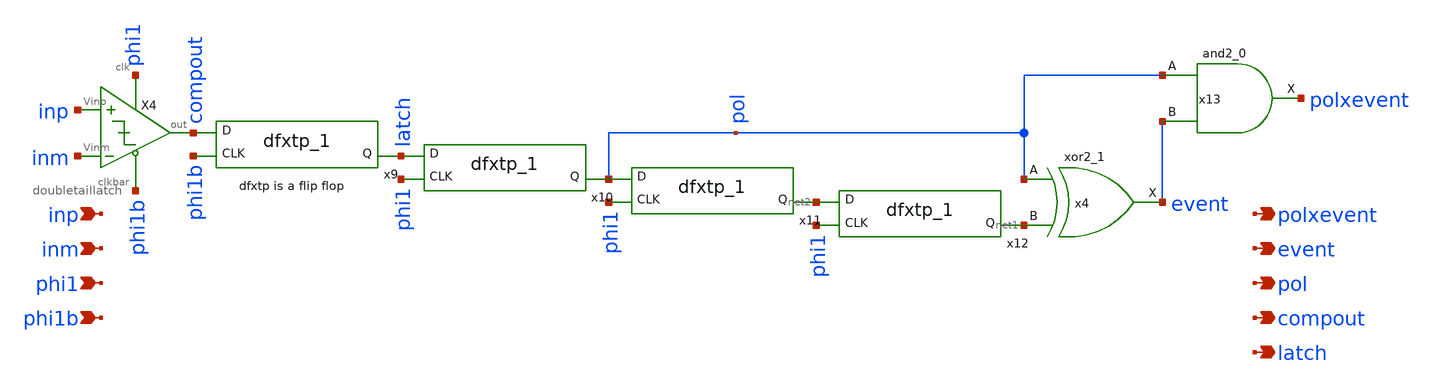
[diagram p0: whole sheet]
** sch_path: xschem/comparator/comparator_out.sch
**.subckt comparator_out inp event polxevent pol inm phi1 phi1b compout latch
*.ipin inp
*.opin event
*.opin polxevent
*.opin pol
*.ipin inm
*.ipin phi1
*.ipin phi1b
*.opin compout
*.opin latch
X4 inp inm compout phi1 phi1b doubletaillatch
x4 pol net1 GND GND VDD VDD event sky130_fd_sc_lp__xor2_1
x11 phi1 pol gnd gnd vdd vdd net2 sky130_fd_sc_lp__dfxtp_1
x12 phi1 net2 gnd gnd vdd vdd net1 sky130_fd_sc_lp__dfxtp_1
x9 phi1b compout gnd gnd vdd vdd latch sky130_fd_sc_lp__dfxtp_1
x10 phi1 latch gnd gnd vdd vdd pol sky130_fd_sc_lp__dfxtp_1
x13 pol event GND GND VDD VDD polxevent sky130_fd_sc_lp__and2_0
**.ends

* expanding   symbol:  comparator/doubletaillatch.sym # of pins=5
** sym_path: xschem/comparator/doubletaillatch.sym
** sch_path: xschem/comparator/doubletaillatch.sch
.subckt doubletaillatch Vinp Vinm out clk clkbar
*.ipin clkbar
*.opin out
*.ipin Vinp
*.ipin Vinm
*.ipin clk
XM3 net6 out VDD VDD sky130_fd_pr__pfet_01v8 L=1 W=4 nf=1 ad='int((nf+1)/2) * W/nf * 0.29' as='int((nf+2)/2) * W/nf * 0.29'
+ pd='2*int((nf+1)/2) * (W/nf + 0.29)' ps='2*int((nf+2)/2) * (W/nf + 0.29)' nrd='0.29 / W' nrs='0.29 / W'
+ sa=0 sb=0 sd=0 mult=1 m=1
XM4 VDD net1 net7 VDD sky130_fd_pr__pfet_01v8 L=1 W=4 nf=1 ad='int((nf+1)/2) * W/nf * 0.29' as='int((nf+2)/2) * W/nf * 0.29'
+ pd='2*int((nf+1)/2) * (W/nf + 0.29)' ps='2*int((nf+2)/2) * (W/nf + 0.29)' nrd='0.29 / W' nrs='0.29 / W'
+ sa=0 sb=0 sd=0 mult=1 m=1
XM5 net7 net3 out VDD sky130_fd_pr__pfet_01v8 L=1 W=4 nf=1 ad='int((nf+1)/2) * W/nf * 0.29' as='int((nf+2)/2) * W/nf * 0.29'
+ pd='2*int((nf+1)/2) * (W/nf + 0.29)' ps='2*int((nf+2)/2) * (W/nf + 0.29)' nrd='0.29 / W' nrs='0.29 / W'
+ sa=0 sb=0 sd=0 mult=1 m=1
XM6 net1 net4 net6 VDD sky130_fd_pr__pfet_01v8 L=1 W=4 nf=1 ad='int((nf+1)/2) * W/nf * 0.29' as='int((nf+2)/2) * W/nf * 0.29'
+ pd='2*int((nf+1)/2) * (W/nf + 0.29)' ps='2*int((nf+2)/2) * (W/nf + 0.29)' nrd='0.29 / W' nrs='0.29 / W'
+ sa=0 sb=0 sd=0 mult=1 m=1
XM7 out clkbar GND GND sky130_fd_pr__nfet_01v8 L=1 W=2 nf=1 ad='int((nf+1)/2) * W/nf * 0.29' as='int((nf+2)/2) * W/nf * 0.29'
+ pd='2*int((nf+1)/2) * (W/nf + 0.29)' ps='2*int((nf+2)/2) * (W/nf + 0.29)' nrd='0.29 / W' nrs='0.29 / W'
+ sa=0 sb=0 sd=0 mult=1 m=1
XM8 GND net1 out GND sky130_fd_pr__nfet_01v8 L=1 W=2 nf=1 ad='int((nf+1)/2) * W/nf * 0.29' as='int((nf+2)/2) * W/nf * 0.29'
+ pd='2*int((nf+1)/2) * (W/nf + 0.29)' ps='2*int((nf+2)/2) * (W/nf + 0.29)' nrd='0.29 / W' nrs='0.29 / W'
+ sa=0 sb=0 sd=0 mult=1 m=1
XM9 net1 out GND GND sky130_fd_pr__nfet_01v8 L=1 W=2 nf=1 ad='int((nf+1)/2) * W/nf * 0.29' as='int((nf+2)/2) * W/nf * 0.29'
+ pd='2*int((nf+1)/2) * (W/nf + 0.29)' ps='2*int((nf+2)/2) * (W/nf + 0.29)' nrd='0.29 / W' nrs='0.29 / W'
+ sa=0 sb=0 sd=0 mult=1 m=1
XM10 GND clkbar net1 GND sky130_fd_pr__nfet_01v8 L=1 W=2 nf=1 ad='int((nf+1)/2) * W/nf * 0.29' as='int((nf+2)/2) * W/nf * 0.29'
+ pd='2*int((nf+1)/2) * (W/nf + 0.29)' ps='2*int((nf+2)/2) * (W/nf + 0.29)' nrd='0.29 / W' nrs='0.29 / W'
+ sa=0 sb=0 sd=0 mult=1 m=1
XM11 net4 clk VDD VDD sky130_fd_pr__pfet_01v8 L=1 W=4 nf=1 ad='int((nf+1)/2) * W/nf * 0.29' as='int((nf+2)/2) * W/nf * 0.29'
+ pd='2*int((nf+1)/2) * (W/nf + 0.29)' ps='2*int((nf+2)/2) * (W/nf + 0.29)' nrd='0.29 / W' nrs='0.29 / W'
+ sa=0 sb=0 sd=0 mult=1 m=1
XM12 VDD clk net3 VDD sky130_fd_pr__pfet_01v8 L=1 W=4 nf=1 ad='int((nf+1)/2) * W/nf * 0.29' as='int((nf+2)/2) * W/nf * 0.29'
+ pd='2*int((nf+1)/2) * (W/nf + 0.29)' ps='2*int((nf+2)/2) * (W/nf + 0.29)' nrd='0.29 / W' nrs='0.29 / W'
+ sa=0 sb=0 sd=0 mult=1 m=1
XM13 net4 Vinm net2 GND sky130_fd_pr__nfet_01v8 L=1 W=2 nf=1 ad='int((nf+1)/2) * W/nf * 0.29' as='int((nf+2)/2) * W/nf * 0.29'
+ pd='2*int((nf+1)/2) * (W/nf + 0.29)' ps='2*int((nf+2)/2) * (W/nf + 0.29)' nrd='0.29 / W' nrs='0.29 / W'
+ sa=0 sb=0 sd=0 mult=1 m=1
XM14 net2 Vinp net3 GND sky130_fd_pr__nfet_01v8 L=1 W=2 nf=1 ad='int((nf+1)/2) * W/nf * 0.29' as='int((nf+2)/2) * W/nf * 0.29'
+ pd='2*int((nf+1)/2) * (W/nf + 0.29)' ps='2*int((nf+2)/2) * (W/nf + 0.29)' nrd='0.29 / W' nrs='0.29 / W'
+ sa=0 sb=0 sd=0 mult=1 m=1
XM15 net2 clk net5 GND sky130_fd_pr__nfet_01v8 L=1 W=2 nf=1 ad='int((nf+1)/2) * W/nf * 0.29' as='int((nf+2)/2) * W/nf * 0.29'
+ pd='2*int((nf+1)/2) * (W/nf + 0.29)' ps='2*int((nf+2)/2) * (W/nf + 0.29)' nrd='0.29 / W' nrs='0.29 / W'
+ sa=0 sb=0 sd=0 mult=1 m=1
XM16 net5 clkbar GND GND sky130_fd_pr__nfet_01v8 L=1 W=2 nf=1 ad='int((nf+1)/2) * W/nf * 0.29' as='int((nf+2)/2) * W/nf * 0.29'
+ pd='2*int((nf+1)/2) * (W/nf + 0.29)' ps='2*int((nf+2)/2) * (W/nf + 0.29)' nrd='0.29 / W' nrs='0.29 / W'
+ sa=0 sb=0 sd=0 mult=1 m=1
XC2 net5 GND sky130_fd_pr__cap_mim_m3_1 W=10 L=10 MF=1 m=1
XC1 net4 GND sky130_fd_pr__cap_mim_m3_1 W=1 L=1 MF=1 m=1
XC3 net3 GND sky130_fd_pr__cap_mim_m3_1 W=1 L=1 MF=1 m=1
.ends

.GLOBAL VDD
.GLOBAL GND
.end
